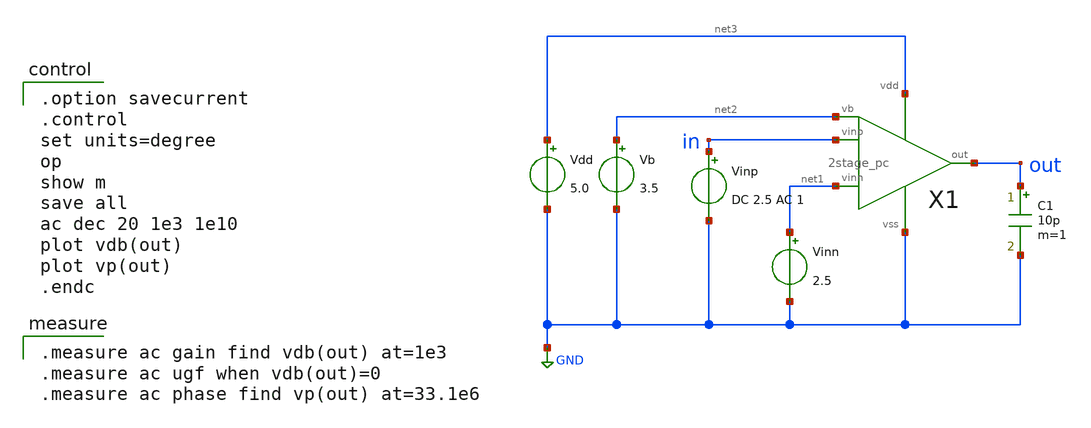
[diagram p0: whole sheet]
** sch_path: OR1/PTC06/opamp/2stage_pc_ac.sch
**.subckt 2stage_pc_ac
Vdd net3 GND 5.0
Vb net2 GND 3.5
Vinn net1 GND 2.5
Vinp in GND DC 2.5 AC 1
C1 out GND 10p m=1
X1 in net1 net2 out net3 GND 2stage_pc
**** begin user architecture code

.option savecurrent
.control
set units=degree
op
show m
save all
ac dec 20 1e3 1e10
plot vdb(out)
plot vp(out)
.endc


.measure ac gain find vdb(out) at=1e3
.measure ac ugf when vdb(out)=0
.measure ac phase find vp(out) at=33.1e6

 .include $::LIB/mos.lib
.include $::LIB/passive.lib
.include $::LIB/diode.lib
**** end user architecture code
**.ends

* expanding   symbol:  2stage_pc.sym # of pins=6
** sym_path: 2stage_pc.sym
** sch_path: 2stage_pc.sch
.subckt 2stage_pc vinp vinn vb out vdd vss
*.ipin vinp
*.ipin vinn
*.ipin vb
*.opin out
*.iopin vdd
*.iopin vss
X1 vinp vinn net2 vdd vss vb diff
X2 net2 vb out vdd vss cs
M2 net3 net1 net2 vss nmos L=2u W=40u m=1
M6 net1 vb vdd vdd pmos L=2u W=20u m=1
M1 net1 net1 net4 vss nmos L=2u W=10u m=1
M7 net4 net4 vss vss nmos L=2u W=10u m=1
C1 out net3 poly_cap W=18 L=18
.ends


* expanding   symbol:  diff.sym # of pins=6
** sym_path: diff.sym
** sch_path: diff.sch
.subckt diff vinp vinn out vdd vss vb
*.ipin vinn
*.ipin vinp
*.ipin vb
*.opin out
*.iopin vdd
*.iopin vss
M5 net2 vb vdd vdd pmos L=2u W=40u m=1
M1 net1 vinn net2 net2 pmos L=2u W=200u m=1
M2 out vinp net2 net2 pmos L=2u W=200u m=1
M3 net1 net1 vss vss nmos L=2u W=10u m=1
M4 out net1 vss vss nmos L=2u W=10u m=1
.ends


* expanding   symbol:  cs.sym # of pins=5
** sym_path: cs.sym
** sch_path: cs.sch
.subckt cs vin vb out vdd vss
*.ipin vb
*.ipin vin
*.opin out
*.iopin vss
*.iopin vdd
M6 out vb vdd vdd pmos L=2u W=400u m=1
M7 out vin vss vss nmos L=2u W=200u m=1
.ends

.GLOBAL GND
.end
